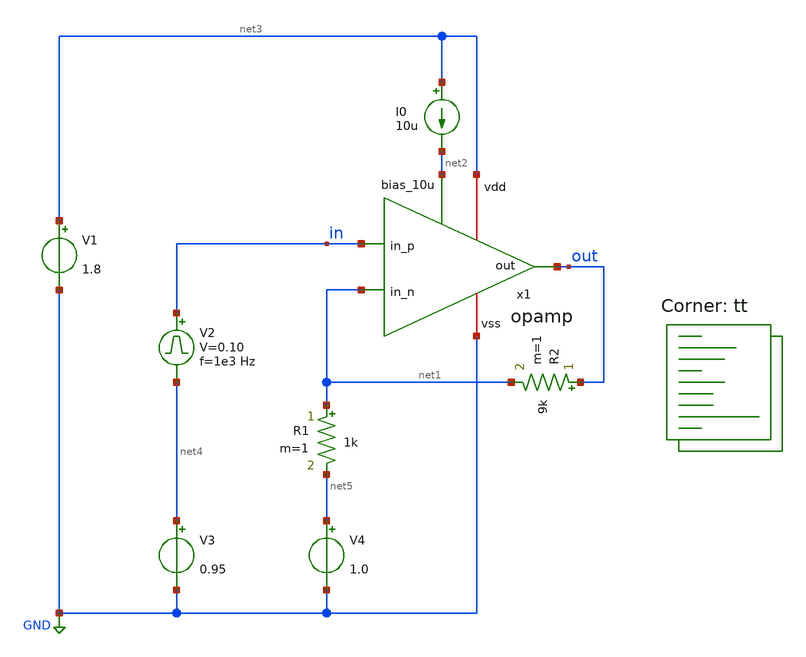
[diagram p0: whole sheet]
** sch_path: design/opamp/test/test_opamp_tran.sch
**.subckt test_opamp_tran
x1 net3 net1 in out net2 GND opamp
I0 net3 net2 10u
V1 net3 GND 1.8
R1 net1 net5 1k m=1
R2 out net1 9k m=1
V2 in net4 pulse 0 0.10 '0.495/ 1e3 ' '0.01/1e3 ' '0.01/1e3 ' '0.49/1e3 ' '1/1e3 '
V3 net4 GND 0.95
V4 net5 GND 1.0
**** begin user architecture code


.param temp=27

*.op
*.ac dec 10 1 10G

.control
tran 1u 10m
plot v(out)
.endc

.save all



.lib $::SKYWATER_MODELS/sky130.lib.spice tt
**** end user architecture code
**.ends

* expanding   symbol:  opamp/opamp.sym # of pins=6
** sym_path: design/opamp/opamp.sym
** sch_path: design/opamp/opamp.sch
.subckt opamp vdd in_n in_p out bias_10u vss
*.iopin vdd
*.iopin vss
*.ipin in_n
*.ipin in_p
*.opin out
*.ipin bias_10u
XM1 bias_10u bias_10u vss vss sky130_fd_pr__nfet_01v8_lvt L=2 W=1 nf=1 ad='int((nf+1)/2) * W/nf * 0.29'
+ as='int((nf+2)/2) * W/nf * 0.29' pd='2*int((nf+1)/2) * (W/nf + 0.29)' ps='2*int((nf+2)/2) * (W/nf + 0.29)'
+ nrd='0.29 / W' nrs='0.29 / W' sa=0 sb=0 sd=0 mult=1 m=1
XM_diff_n net3 in_n net1 vss sky130_fd_pr__nfet_01v8_lvt L=1 W=9 nf=1 ad='int((nf+1)/2) * W/nf * 0.29'
+ as='int((nf+2)/2) * W/nf * 0.29' pd='2*int((nf+1)/2) * (W/nf + 0.29)' ps='2*int((nf+2)/2) * (W/nf + 0.29)'
+ nrd='0.29 / W' nrs='0.29 / W' sa=0 sb=0 sd=0 mult=2 m=2
XM_diff_n1 net4 in_p net1 vss sky130_fd_pr__nfet_01v8_lvt L=1 W=9 nf=1 ad='int((nf+1)/2) * W/nf * 0.29'
+ as='int((nf+2)/2) * W/nf * 0.29' pd='2*int((nf+1)/2) * (W/nf + 0.29)' ps='2*int((nf+2)/2) * (W/nf + 0.29)'
+ nrd='0.29 / W' nrs='0.29 / W' sa=0 sb=0 sd=0 mult=2 m=2
XM_tail net1 net2 vss vss sky130_fd_pr__nfet_01v8_lvt L=4 W=5 nf=1 ad='int((nf+1)/2) * W/nf * 0.29' as='int((nf+2)/2) * W/nf * 0.29'
+ pd='2*int((nf+1)/2) * (W/nf + 0.29)' ps='2*int((nf+2)/2) * (W/nf + 0.29)' nrd='0.29 / W' nrs='0.29 / W'
+ sa=0 sb=0 sd=0 mult=8 m=8
XM_actload out net2 vss vss sky130_fd_pr__nfet_01v8_lvt L=2 W=4 nf=1 ad='int((nf+1)/2) * W/nf * 0.29'
+ as='int((nf+2)/2) * W/nf * 0.29' pd='2*int((nf+1)/2) * (W/nf + 0.29)' ps='2*int((nf+2)/2) * (W/nf + 0.29)'
+ nrd='0.29 / W' nrs='0.29 / W' sa=0 sb=0 sd=0 mult=6 m=6
XM_ppair_p net4 net3 vdd vdd sky130_fd_pr__pfet_01v8_lvt L=2 W=8 nf=1 ad='int((nf+1)/2) * W/nf * 0.29'
+ as='int((nf+2)/2) * W/nf * 0.29' pd='2*int((nf+1)/2) * (W/nf + 0.29)' ps='2*int((nf+2)/2) * (W/nf + 0.29)'
+ nrd='0.29 / W' nrs='0.29 / W' sa=0 sb=0 sd=0 mult=8 m=8
XM_ppair_p1 net3 net3 vdd vdd sky130_fd_pr__pfet_01v8_lvt L=2 W=8 nf=1 ad='int((nf+1)/2) * W/nf * 0.29'
+ as='int((nf+2)/2) * W/nf * 0.29' pd='2*int((nf+1)/2) * (W/nf + 0.29)' ps='2*int((nf+2)/2) * (W/nf + 0.29)'
+ nrd='0.29 / W' nrs='0.29 / W' sa=0 sb=0 sd=0 mult=8 m=8
XM_cs out net4 vdd vdd sky130_fd_pr__pfet_01v8_lvt L=0.5 W=12 nf=1 ad='int((nf+1)/2) * W/nf * 0.29' as='int((nf+2)/2) * W/nf * 0.29'
+ pd='2*int((nf+1)/2) * (W/nf + 0.29)' ps='2*int((nf+2)/2) * (W/nf + 0.29)' nrd='0.29 / W' nrs='0.29 / W'
+ sa=0 sb=0 sd=0 mult=12 m=12
V1 net2 vss 0.7
C1 net4 net5 150f m=1
R1 out net5 400 m=1
.ends

.GLOBAL GND
.end
